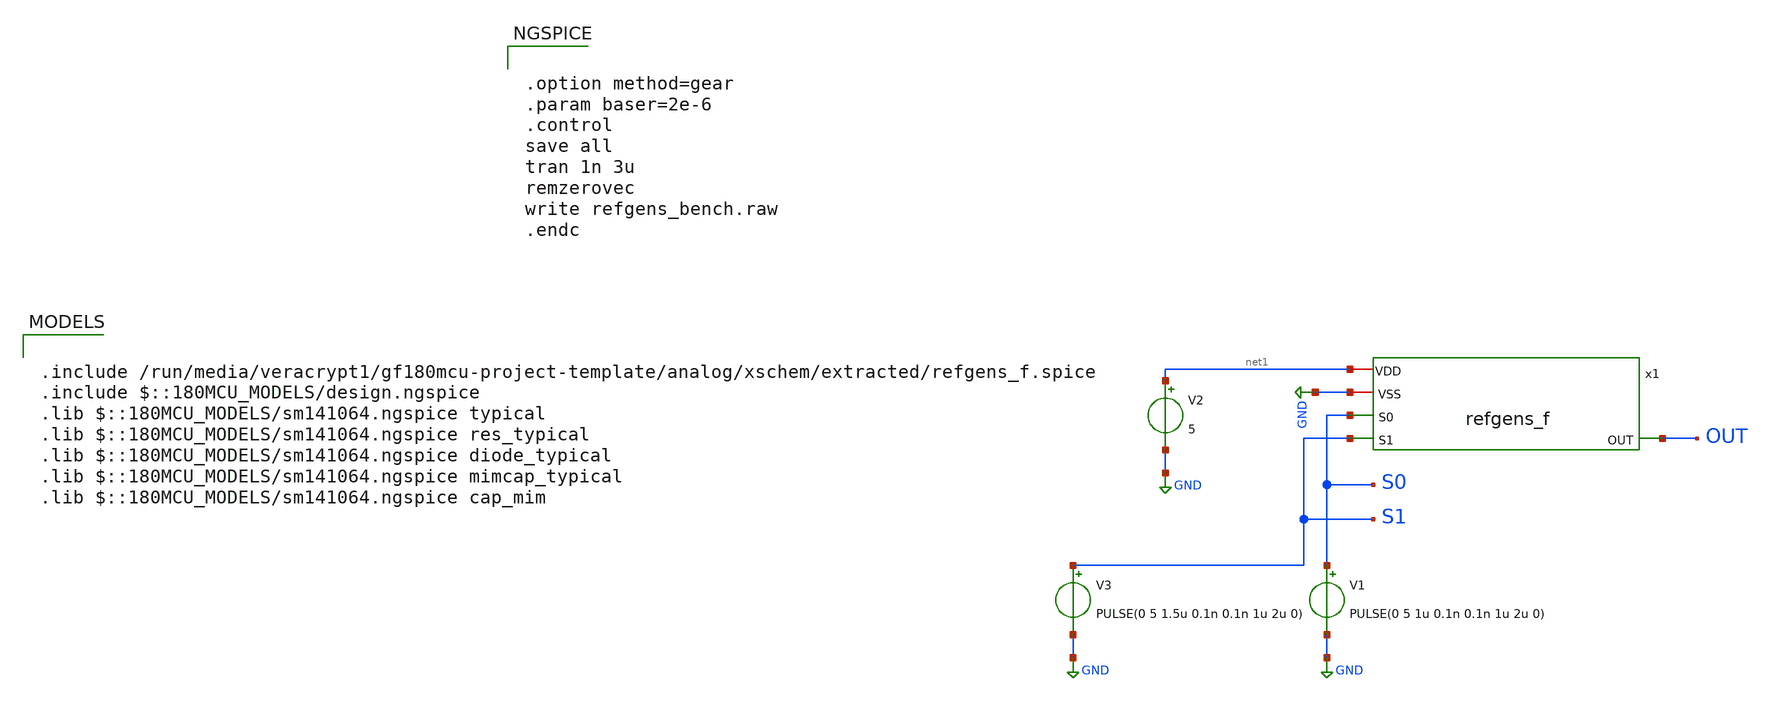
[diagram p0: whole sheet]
** sch_path: analog/xschem/refgens_bench.sch
**.subckt refgens_bench
V2 net1 GND 5
V1 S0 GND PULSE(0 5 1u 0.1n 0.1n 1u 2u 0)
V3 S1 GND PULSE(0 5 1.5u 0.1n 0.1n 1u 2u 0)
x1 net1 GND S0 S1 OUT refgens_f
**** begin user architecture code


.option method=gear
.param baser=2e-6
.control
save all
tran 1n 3u
remzerovec
write refgens_bench.raw
.endc



.include /run/media/veracrypt1/gf180mcu-project-template/analog/xschem/extracted/refgens_f.spice
.include $::180MCU_MODELS/design.ngspice
.lib $::180MCU_MODELS/sm141064.ngspice typical
.lib $::180MCU_MODELS/sm141064.ngspice res_typical
.lib $::180MCU_MODELS/sm141064.ngspice diode_typical
.lib $::180MCU_MODELS/sm141064.ngspice mimcap_typical
.lib $::180MCU_MODELS/sm141064.ngspice cap_mim

**** end user architecture code
**.ends
.GLOBAL GND
.end
